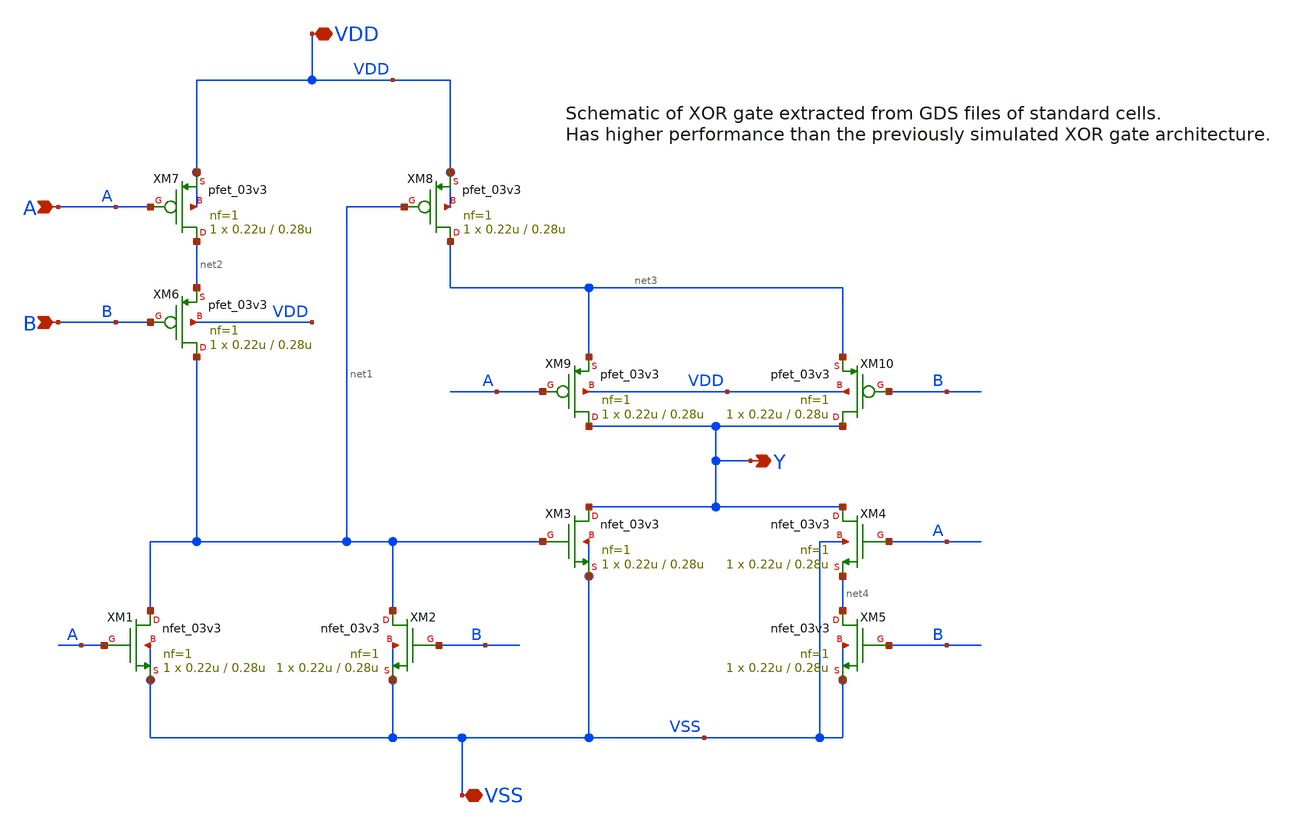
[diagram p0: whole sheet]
** sch_path: src/UN_PFD_GF180mcuD/work/UN_stdXOR_0_gf180mcuD.sch
**.subckt UN_stdXOR_0_gf180mcuD VDD VSS A B Y
*.iopin VDD
*.iopin VSS
*.ipin A
*.ipin B
*.opin Y
XM1 net1 A VSS VSS nfet_03v3 L=0.28u W=0.22u nf=1 ad='int((nf+1)/2) * W/nf * 0.18u' as='int((nf+2)/2) * W/nf * 0.18u'
+ pd='2*int((nf+1)/2) * (W/nf + 0.18u)' ps='2*int((nf+2)/2) * (W/nf + 0.18u)' nrd='0.18u / W' nrs='0.18u / W'
+ sa=0 sb=0 sd=0 m=1
XM2 net1 B VSS VSS nfet_03v3 L=0.28u W=0.22u nf=1 ad='int((nf+1)/2) * W/nf * 0.18u' as='int((nf+2)/2) * W/nf * 0.18u'
+ pd='2*int((nf+1)/2) * (W/nf + 0.18u)' ps='2*int((nf+2)/2) * (W/nf + 0.18u)' nrd='0.18u / W' nrs='0.18u / W'
+ sa=0 sb=0 sd=0 m=1
XM3 Y net1 VSS VSS nfet_03v3 L=0.28u W=0.22u nf=1 ad='int((nf+1)/2) * W/nf * 0.18u' as='int((nf+2)/2) * W/nf * 0.18u'
+ pd='2*int((nf+1)/2) * (W/nf + 0.18u)' ps='2*int((nf+2)/2) * (W/nf + 0.18u)' nrd='0.18u / W' nrs='0.18u / W'
+ sa=0 sb=0 sd=0 m=1
XM4 Y A net4 VSS nfet_03v3 L=0.28u W=0.22u nf=1 ad='int((nf+1)/2) * W/nf * 0.18u' as='int((nf+2)/2) * W/nf * 0.18u'
+ pd='2*int((nf+1)/2) * (W/nf + 0.18u)' ps='2*int((nf+2)/2) * (W/nf + 0.18u)' nrd='0.18u / W' nrs='0.18u / W'
+ sa=0 sb=0 sd=0 m=1
XM5 net4 B VSS VSS nfet_03v3 L=0.28u W=0.22u nf=1 ad='int((nf+1)/2) * W/nf * 0.18u' as='int((nf+2)/2) * W/nf * 0.18u'
+ pd='2*int((nf+1)/2) * (W/nf + 0.18u)' ps='2*int((nf+2)/2) * (W/nf + 0.18u)' nrd='0.18u / W' nrs='0.18u / W'
+ sa=0 sb=0 sd=0 m=1
XM6 net1 B net2 VDD pfet_03v3 L=0.28u W=0.22u nf=1 ad='int((nf+1)/2) * W/nf * 0.18u' as='int((nf+2)/2) * W/nf * 0.18u'
+ pd='2*int((nf+1)/2) * (W/nf + 0.18u)' ps='2*int((nf+2)/2) * (W/nf + 0.18u)' nrd='0.18u / W' nrs='0.18u / W'
+ sa=0 sb=0 sd=0 m=1
XM7 net2 A VDD VDD pfet_03v3 L=0.28u W=0.22u nf=1 ad='int((nf+1)/2) * W/nf * 0.18u' as='int((nf+2)/2) * W/nf * 0.18u'
+ pd='2*int((nf+1)/2) * (W/nf + 0.18u)' ps='2*int((nf+2)/2) * (W/nf + 0.18u)' nrd='0.18u / W' nrs='0.18u / W'
+ sa=0 sb=0 sd=0 m=1
XM8 net3 net1 VDD VDD pfet_03v3 L=0.28u W=0.22u nf=1 ad='int((nf+1)/2) * W/nf * 0.18u' as='int((nf+2)/2) * W/nf * 0.18u'
+ pd='2*int((nf+1)/2) * (W/nf + 0.18u)' ps='2*int((nf+2)/2) * (W/nf + 0.18u)' nrd='0.18u / W' nrs='0.18u / W'
+ sa=0 sb=0 sd=0 m=1
XM9 Y A net3 VDD pfet_03v3 L=0.28u W=0.22u nf=1 ad='int((nf+1)/2) * W/nf * 0.18u' as='int((nf+2)/2) * W/nf * 0.18u'
+ pd='2*int((nf+1)/2) * (W/nf + 0.18u)' ps='2*int((nf+2)/2) * (W/nf + 0.18u)' nrd='0.18u / W' nrs='0.18u / W'
+ sa=0 sb=0 sd=0 m=1
XM10 Y B net3 VDD pfet_03v3 L=0.28u W=0.22u nf=1 ad='int((nf+1)/2) * W/nf * 0.18u' as='int((nf+2)/2) * W/nf * 0.18u'
+ pd='2*int((nf+1)/2) * (W/nf + 0.18u)' ps='2*int((nf+2)/2) * (W/nf + 0.18u)' nrd='0.18u / W' nrs='0.18u / W'
+ sa=0 sb=0 sd=0 m=1
**.ends
.end
